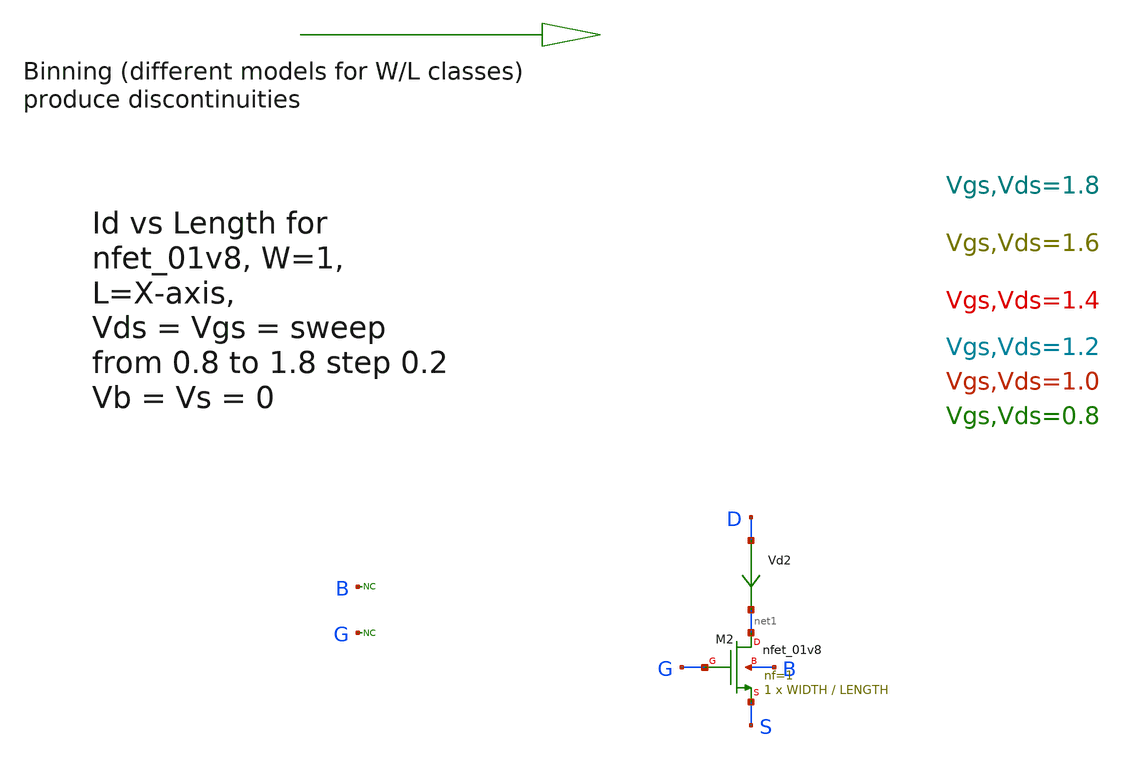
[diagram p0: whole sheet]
** sch_path: sky130A/xschem_libs/sky130_tests_ase/test_mos_binning/schematic/test_mos_binning.sch
* Copyright 2021 Stefan Frederik Schippers
* Licensed under the Apache License, Version 2.0 (the "License");
* you may not use this file except in compliance with the License.
* You may obtain a copy of the License at
* https://www.apache.org/licenses/LICENSE-2.0
* Unless required by applicable law or agreed to in writing, software
* distributed under the License is distributed on an "AS IS" BASIS,
* WITHOUT WARRANTIES OR CONDITIONS OF ANY KIND, either express or implied.
* See the License for the specific language governing permissions and
* limitations under the License.
**.subckt test_mos_binning
Vd2 D net1 0
.save i(vd2)
XM2 net1 G S B sky130_fd_pr__nfet_01v8 L=LENGTH W=WIDTH nf=1 ad='int((1 + 1)/2) * WIDTH / 1 * 0.29' as='int((1 + 2)/2) * WIDTH / 1 * 0.29'
+ pd='2*int((1 + 1)/2) * (WIDTH / 1 + 0.29)' ps='2*int((1 + 2)/2) * (WIDTH / 1 + 0.29)' nrd='0.29 / WIDTH '
+ nrs='0.29 / WIDTH ' sa=0 sb=0 sd=0 mult=1 m=1
* noconn B
* noconn G
**** begin user architecture code


vd d 0 {VGATE}
vg g 0 {VGATE}
vs s 0 0
vb b 0 0


**** end user architecture code
**.ends
.end
